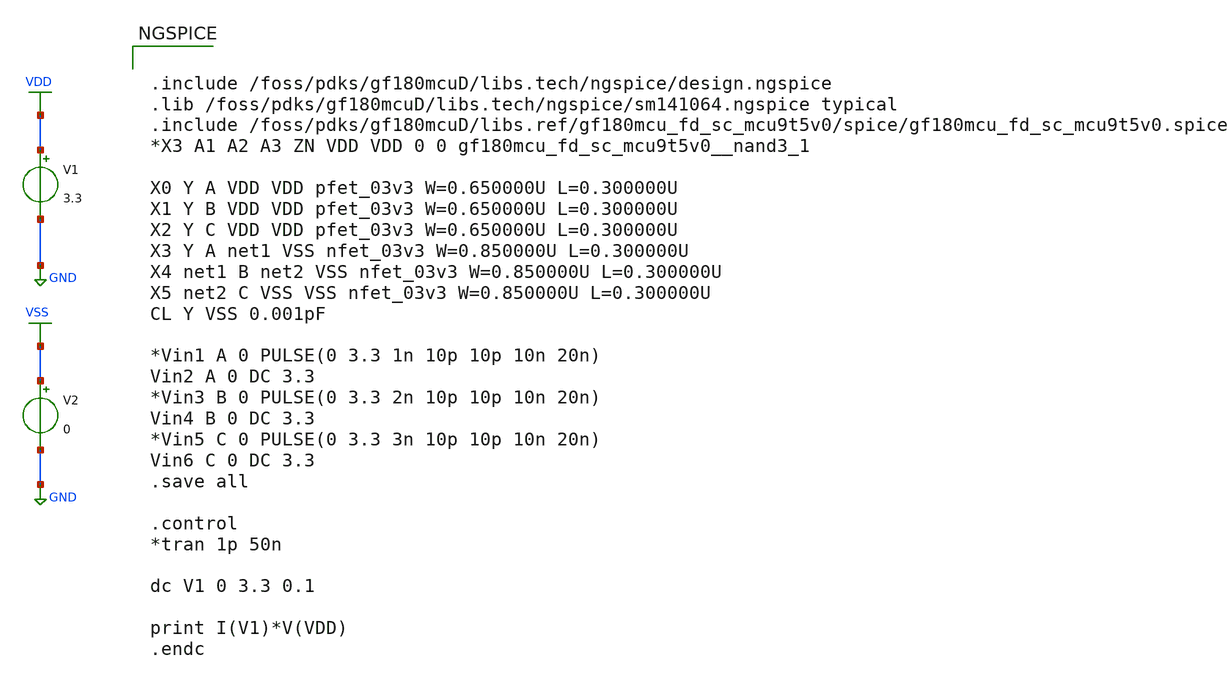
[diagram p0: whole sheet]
** sch_path: designs/libs/tb_NAND3/nand3_test_LP.sch
**.subckt nand3_test_LP
V1 VDD GND 3.3
V2 VSS GND 0
**** begin user architecture code


.include /foss/pdks/gf180mcuD/libs.tech/ngspice/design.ngspice
.lib /foss/pdks/gf180mcuD/libs.tech/ngspice/sm141064.ngspice typical
.include /foss/pdks/gf180mcuD/libs.ref/gf180mcu_fd_sc_mcu9t5v0/spice/gf180mcu_fd_sc_mcu9t5v0.spice
*X3 A1 A2 A3 ZN VDD VDD 0 0 gf180mcu_fd_sc_mcu9t5v0__nand3_1

X0 Y A VDD VDD pfet_03v3 W=0.650000U L=0.300000U
X1 Y B VDD VDD pfet_03v3 W=0.650000U L=0.300000U
X2 Y C VDD VDD pfet_03v3 W=0.650000U L=0.300000U
X3 Y A net1 VSS nfet_03v3 W=0.850000U L=0.300000U
X4 net1 B net2 VSS nfet_03v3 W=0.850000U L=0.300000U
X5 net2 C VSS VSS nfet_03v3 W=0.850000U L=0.300000U
CL Y VSS 0.001pF

*Vin1 A 0 PULSE(0 3.3 1n 10p 10p 10n 20n)
Vin2 A 0 DC 3.3
*Vin3 B 0 PULSE(0 3.3 2n 10p 10p 10n 20n)
Vin4 B 0 DC 3.3
*Vin5 C 0 PULSE(0 3.3 3n 10p 10p 10n 20n)
Vin6 C 0 DC 3.3
.save all

.control
*tran 1p 50n

dc V1 0 3.3 0.1

print I(V1)*V(VDD)
.endc


**** end user architecture code
**.ends
.GLOBAL VDD
.GLOBAL GND
.GLOBAL VSS
.end
